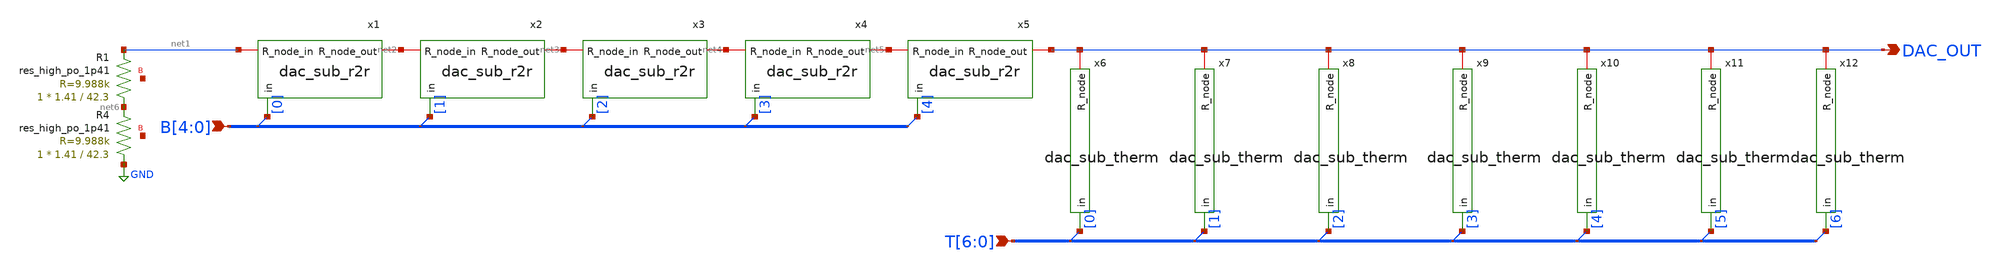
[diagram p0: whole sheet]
** sch_path: xschem/dac_seg_5_3.sch
**.subckt dac_seg_5_3 B[4],B[3],B[2],B[1],B[0] T[6],T[5],T[4],T[3],T[2],T[1],T[0] DAC_OUT
*.ipin B[4],B[3],B[2],B[1],B[0]
*.ipin T[6],T[5],T[4],T[3],T[2],T[1],T[0]
*.opin DAC_OUT
x1 net2 net1 B[0] dac_sub_r2r
x2 net3 net2 B[1] dac_sub_r2r
x3 net4 net3 B[2] dac_sub_r2r
x4 net5 net4 B[3] dac_sub_r2r
x5 DAC_OUT net5 B[4] dac_sub_r2r
* tap: B[4:0] --> B[0]
* tap: B[4:0] --> B[1]
* tap: B[4:0] --> B[2]
* tap: B[4:0] --> B[3]
* tap: B[4:0] --> B[4]
XR1 net6 net1 net7 sky130_fd_pr__res_high_po_1p41 L=42.3 mult=1 m=1
XR4 GND net6 net8 sky130_fd_pr__res_high_po_1p41 L=42.3 mult=1 m=1
x6 DAC_OUT T[0] dac_sub_therm
x7 DAC_OUT T[1] dac_sub_therm
x8 DAC_OUT T[2] dac_sub_therm
x9 DAC_OUT T[3] dac_sub_therm
x10 DAC_OUT T[4] dac_sub_therm
x11 DAC_OUT T[5] dac_sub_therm
x12 DAC_OUT T[6] dac_sub_therm
* tap: T[6:0] --> T[0]
* tap: T[6:0] --> T[1]
* tap: T[6:0] --> T[2]
* tap: T[6:0] --> T[3]
* tap: T[6:0] --> T[4]
* tap: T[6:0] --> T[5]
* tap: T[6:0] --> T[6]
**.ends

* expanding   symbol:  dac_sub_r2r.sym # of pins=3
** sym_path: xschem/dac_sub_r2r.sym
** sch_path: xschem/dac_sub_r2r.sch
.subckt dac_sub_r2r R_node_out R_node_in in
*.ipin in
*.iopin R_node_out
*.iopin R_node_in
XR1 net1 R_node_in GND sky130_fd_pr__res_high_po_1p41 L=42.3 mult=1 m=1
XR2 net2 R_node_in GND sky130_fd_pr__res_high_po_1p41 L=42.3 mult=1 m=1
XR3 net3 R_node_in GND sky130_fd_pr__res_high_po_1p41 L=42.3 mult=1 m=1
XR4 in net1 GND sky130_fd_pr__res_high_po_1p41 L=42.3 mult=1 m=1
XR5 R_node_out net2 GND sky130_fd_pr__res_high_po_1p41 L=42.3 mult=1 m=1
XR6 R_node_out net3 GND sky130_fd_pr__res_high_po_1p41 L=42.3 mult=1 m=1
.ends


* expanding   symbol:  dac_sub_therm.sym # of pins=2
** sym_path: xschem/dac_sub_therm.sym
** sch_path: xschem/dac_sub_therm.sch
.subckt dac_sub_therm R_node in
*.ipin in
*.iopin R_node
XR1 net1 R_node GND sky130_fd_pr__res_high_po_1p41 L=42.3 mult=1 m=1
XR4 in net1 GND sky130_fd_pr__res_high_po_1p41 L=42.3 mult=1 m=1
.ends

.GLOBAL GND
.end
